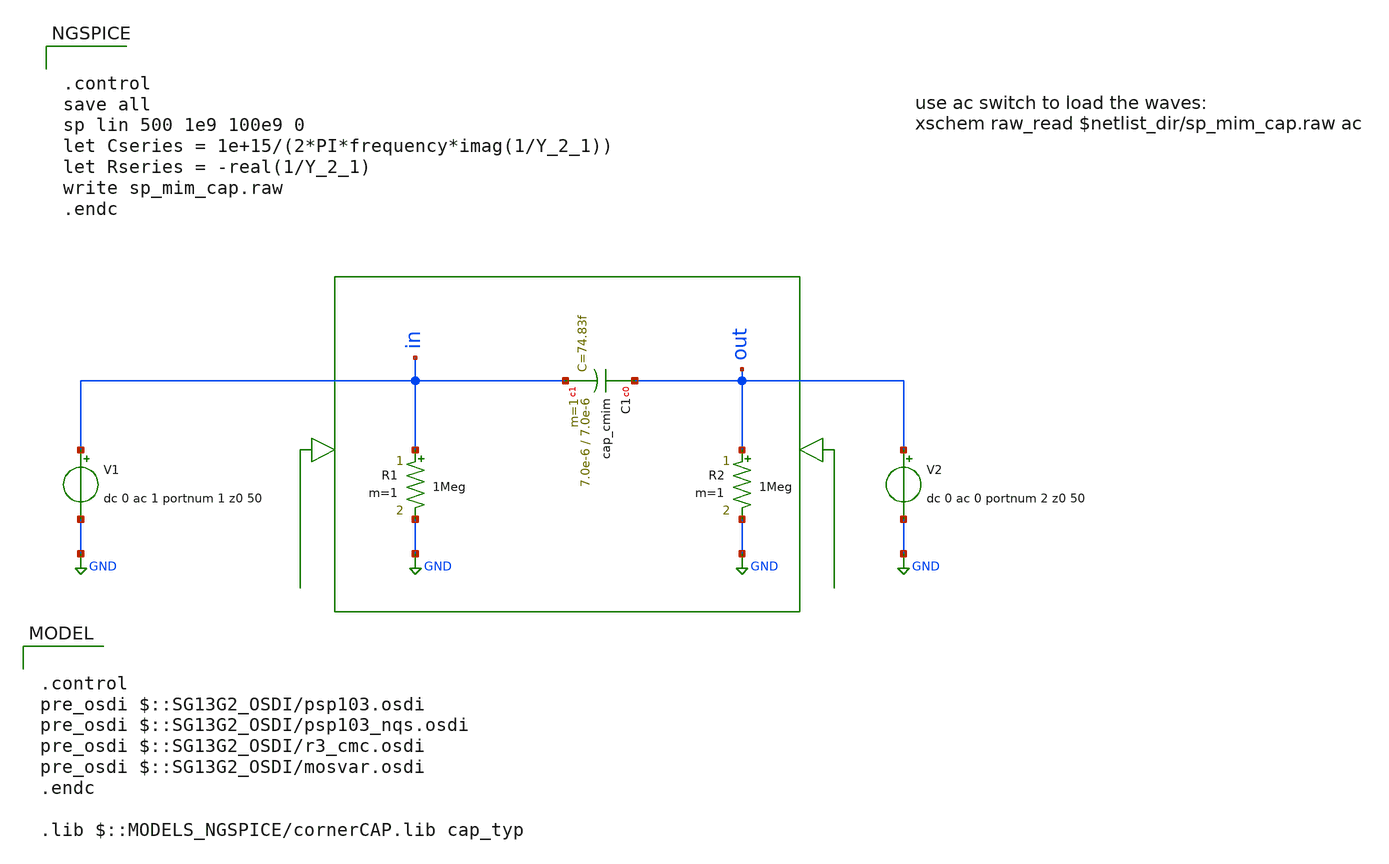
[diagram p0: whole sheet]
** sch_path: ihp-sg13g2/xschem_libs/sg13g2_tests/sp_mim_cap/schematic/sp_mim_cap.sch
* Copyright 2021 Stefan Frederik Schippers
* Licensed under the Apache License, Version 2.0 (the "License");
* you may not use this file except in compliance with the License.
* You may obtain a copy of the License at
* https://www.apache.org/licenses/LICENSE-2.0
* Unless required by applicable law or agreed to in writing, software
* distributed under the License is distributed on an "AS IS" BASIS,
* WITHOUT WARRANTIES OR CONDITIONS OF ANY KIND, either express or implied.
* See the License for the specific language governing permissions and
* limitations under the License.
* Copyright 2023 IHP PDK Authors
**.subckt sp_mim_cap
R1 in GND 1Meg m=1
V1 in GND dc 0 ac 1 portnum 1 z0 50
R2 out GND 1Meg m=1
V2 out GND dc 0 ac 0 portnum 2 z0 50
XC1 out in cap_cmim w=7.0e-6 l=7.0e-6 m=1 mm_ok=1
**** begin user architecture code


.control
save all
sp lin 500 1e9 100e9 0
let Cseries = 1e+15/(2*PI*frequency*imag(1/Y_2_1))
let Rseries = -real(1/Y_2_1)
write sp_mim_cap.raw
.endc



.control
pre_osdi $::SG13G2_OSDI/psp103.osdi
pre_osdi $::SG13G2_OSDI/psp103_nqs.osdi
pre_osdi $::SG13G2_OSDI/r3_cmc.osdi
pre_osdi $::SG13G2_OSDI/mosvar.osdi
.endc

.lib $::MODELS_NGSPICE/cornerCAP.lib cap_typ

**** end user architecture code
**.ends
.GLOBAL GND
.end
